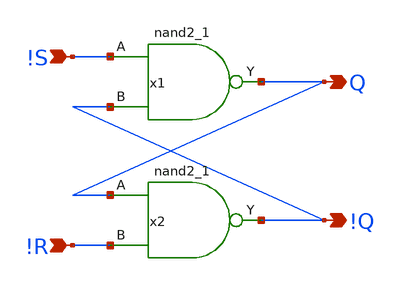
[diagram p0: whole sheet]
** sch_path: RSlatch/xschem/RSandsym.sch
**.subckt RSandsym !S !R Q !Q
*.ipin !S
*.ipin !R
*.opin Q
*.opin !Q
x1 !S !Q GND GND VDD VDD Q sky130_fd_sc_hd__nand2_1
x2 Q !R GND GND VDD VDD !Q sky130_fd_sc_hd__nand2_1
**.ends
.end
